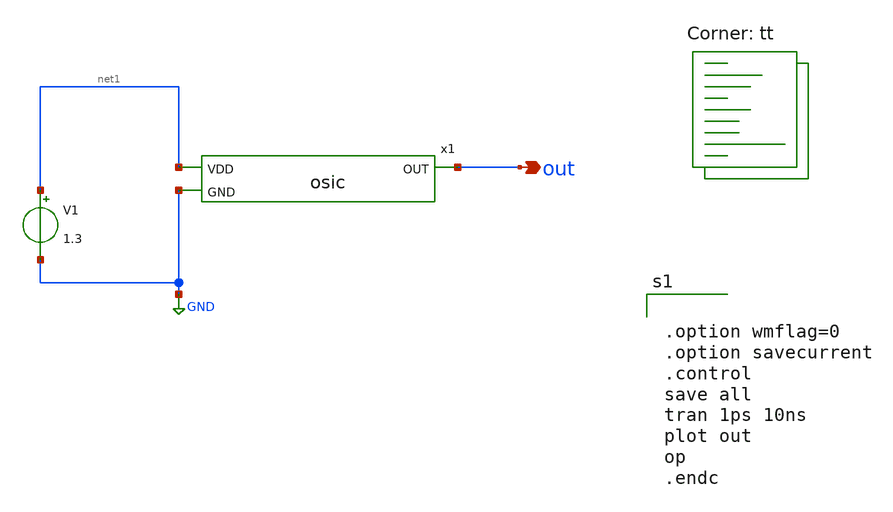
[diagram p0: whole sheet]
** sch_path: tes_o.sch
**.subckt tes_o out
*.opin out
x1 net1 out GND osic
V1 net1 GND 1.3
**** begin user architecture code


.option wmflag=0
.option savecurrent
.control
save all
tran 1ps 10ns
plot out
op
.endc


.lib $::SKYWATER_MODELS/sky130.lib.spice tt
**** end user architecture code
**.ends

* expanding   symbol:  /home/tiredcrab/MSIB/inverter/osic.sym # of pins=3
** sym_path: osic.sym
** sch_path: osic.sch
.subckt osic VDD OUT GND
*.ipin GND
*.ipin VDD
*.opin OUT
x1 VDD OUT net1 GND inverter
x2 VDD net1 net2 GND inverter
x3 VDD net2 OUT GND inverter
.ends


* expanding   symbol:  inverter.sym # of pins=4
** sym_path: inverter.sym
** sch_path: inverter.sch
.subckt inverter VDD in OUT GND
*.ipin in
*.ipin VDD
*.ipin GND
*.opin OUT
XM1 OUT in GND GND sky130_fd_pr__nfet_01v8 L=0.15 W=1 nf=1 ad='int((nf+1)/2) * W/nf * 0.29' as='int((nf+2)/2) * W/nf * 0.29'
+ pd='2*int((nf+1)/2) * (W/nf + 0.29)' ps='2*int((nf+2)/2) * (W/nf + 0.29)' nrd='0.29 / W' nrs='0.29 / W'
+ sa=0 sb=0 sd=0 mult=1 m=1
XM2 OUT in VDD VDD sky130_fd_pr__pfet_01v8 L=0.15 W=1 nf=1 ad='int((nf+1)/2) * W/nf * 0.29' as='int((nf+2)/2) * W/nf * 0.29'
+ pd='2*int((nf+1)/2) * (W/nf + 0.29)' ps='2*int((nf+2)/2) * (W/nf + 0.29)' nrd='0.29 / W' nrs='0.29 / W'
+ sa=0 sb=0 sd=0 mult=1 m=1
.ends

.GLOBAL GND
.end
